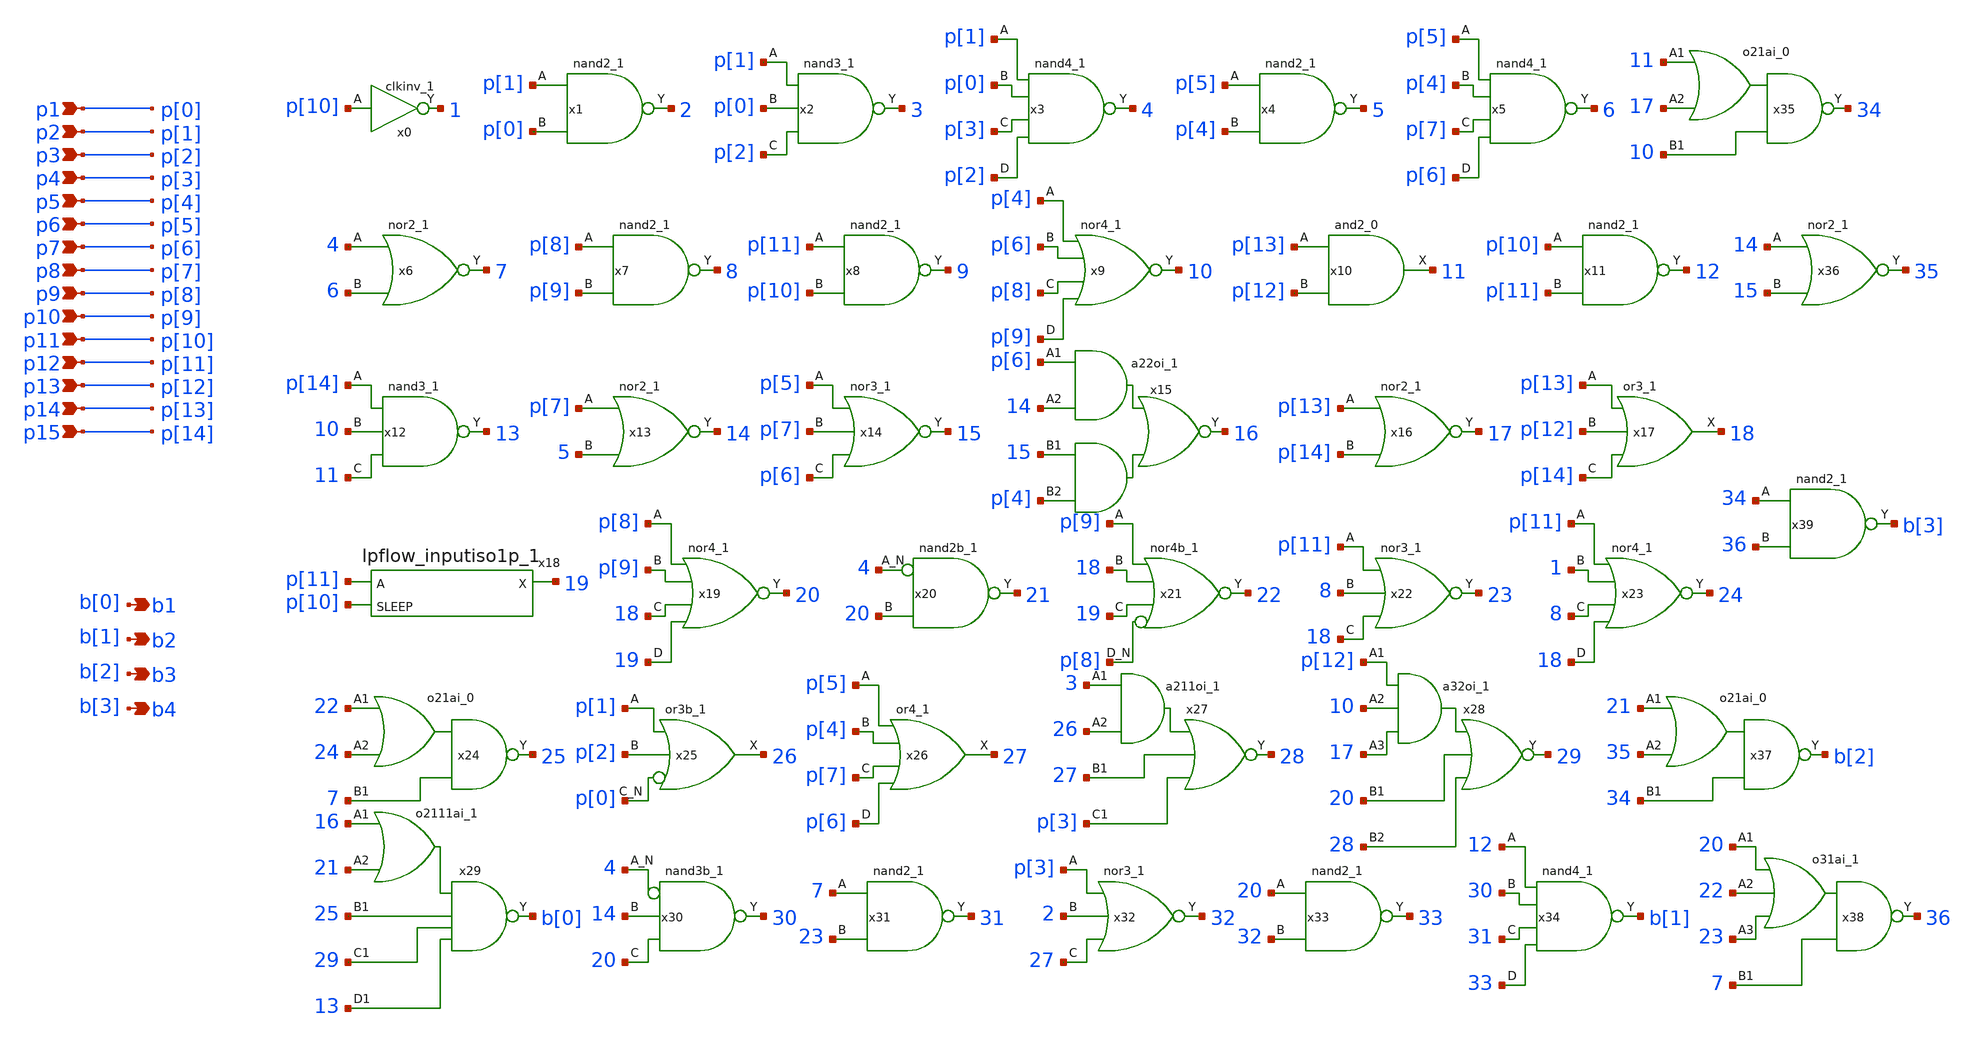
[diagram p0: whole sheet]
** sch_path: xschem/Vth_sch/Symbol/therm1.sch
**.subckt therm1 p1 b1 p2 p3 p4 p5 p6 p7 p8 p9 p10 p11 p12 p13 p14 p15 b2 b3 b4
*.ipin p1
*.opin b1
*.ipin p2
*.ipin p3
*.ipin p4
*.ipin p5
*.ipin p6
*.ipin p7
*.ipin p8
*.ipin p9
*.ipin p10
*.ipin p11
*.ipin p12
*.ipin p13
*.ipin p14
*.ipin p15
*.opin b2
*.opin b3
*.opin b4
x0 p[10] VGND VNB VPB VPWR 1 sky130_fd_sc_hd__clkinv_1
x1 p[1] p[0] VGND VNB VPB VPWR 2 sky130_fd_sc_hd__nand2_1
x2 p[1] p[0] p[2] VGND VNB VPB VPWR 3 sky130_fd_sc_hd__nand3_1
x3 p[1] p[0] p[3] p[2] VGND VNB VPB VPWR 4 sky130_fd_sc_hd__nand4_1
x4 p[5] p[4] VGND VNB VPB VPWR 5 sky130_fd_sc_hd__nand2_1
x5 p[5] p[4] p[7] p[6] VGND VNB VPB VPWR 6 sky130_fd_sc_hd__nand4_1
x6 4 6 VGND VNB VPB VPWR 7 sky130_fd_sc_hd__nor2_1
x7 p[8] p[9] VGND VNB VPB VPWR 8 sky130_fd_sc_hd__nand2_1
x8 p[11] p[10] VGND VNB VPB VPWR 9 sky130_fd_sc_hd__nand2_1
x9 p[4] p[6] p[8] p[9] VGND VNB VPB VPWR 10 sky130_fd_sc_hd__nor4_1
x10 p[13] p[12] VGND VNB VPB VPWR 11 sky130_fd_sc_hd__and2_0
x11 p[10] p[11] VGND VNB VPB VPWR 12 sky130_fd_sc_hd__nand2_1
x12 p[14] 10 11 VGND VNB VPB VPWR 13 sky130_fd_sc_hd__nand3_1
x13 p[7] 5 VGND VNB VPB VPWR 14 sky130_fd_sc_hd__nor2_1
x14 p[5] p[7] p[6] VGND VNB VPB VPWR 15 sky130_fd_sc_hd__nor3_1
x15 p[6] 14 15 p[4] VGND VNB VPB VPWR 16 sky130_fd_sc_hd__a22oi_1
x16 p[13] p[14] VGND VNB VPB VPWR 17 sky130_fd_sc_hd__nor2_1
x17 p[13] p[12] p[14] VGND VNB VPB VPWR 18 sky130_fd_sc_hd__or3_1
x18 p[11] p[10] VGND VNB VPB VPWR 19 sky130_fd_sc_hd__lpflow_inputiso1p_1
x19 p[8] p[9] 18 19 VGND VNB VPB VPWR 20 sky130_fd_sc_hd__nor4_1
x20 4 20 VGND VNB VPB VPWR 21 sky130_fd_sc_hd__nand2b_1
x21 p[9] 18 19 p[8] VGND VNB VPB VPWR 22 sky130_fd_sc_hd__nor4b_1
x22 p[11] 8 18 VGND VNB VPB VPWR 23 sky130_fd_sc_hd__nor3_1
x23 p[11] 1 8 18 VGND VNB VPB VPWR 24 sky130_fd_sc_hd__nor4_1
x24 22 24 7 VGND VNB VPB VPWR 25 sky130_fd_sc_hd__o21ai_0
x25 p[1] p[2] p[0] VGND VNB VPB VPWR 26 sky130_fd_sc_hd__or3b_1
x26 p[5] p[4] p[7] p[6] VGND VNB VPB VPWR 27 sky130_fd_sc_hd__or4_1
x27 3 26 27 p[3] VGND VNB VPB VPWR 28 sky130_fd_sc_hd__a211oi_1
x28 p[12] 10 17 20 28 VGND VNB VPB VPWR 29 sky130_fd_sc_hd__a32oi_1
x29 16 21 25 29 13 VGND VNB VPB VPWR b[0] sky130_fd_sc_hd__o2111ai_1
x30 4 14 20 VGND VNB VPB VPWR 30 sky130_fd_sc_hd__nand3b_1
x31 7 23 VGND VNB VPB VPWR 31 sky130_fd_sc_hd__nand2_1
x32 p[3] 2 27 VGND VNB VPB VPWR 32 sky130_fd_sc_hd__nor3_1
x33 20 32 VGND VNB VPB VPWR 33 sky130_fd_sc_hd__nand2_1
x34 12 30 31 33 VGND VNB VPB VPWR b[1] sky130_fd_sc_hd__nand4_1
x35 11 17 10 VGND VNB VPB VPWR 34 sky130_fd_sc_hd__o21ai_0
x36 14 15 VGND VNB VPB VPWR 35 sky130_fd_sc_hd__nor2_1
x37 21 35 34 VGND VNB VPB VPWR b[2] sky130_fd_sc_hd__o21ai_0
x38 20 22 23 7 VGND VNB VPB VPWR 36 sky130_fd_sc_hd__o31ai_1
x39 34 36 VGND VNB VPB VPWR b[3] sky130_fd_sc_hd__nand2_1
**.ends
.end
